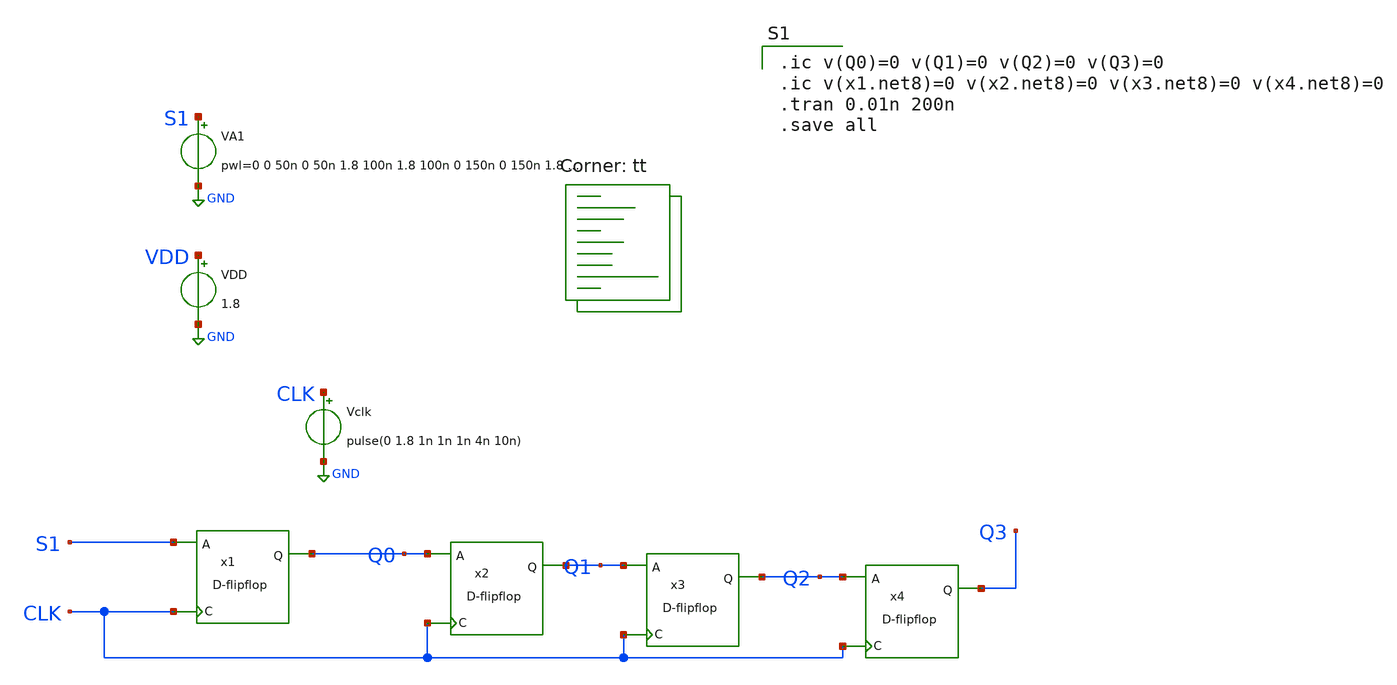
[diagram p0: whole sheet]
** sch_path: gates/dflipshift4bitsim.sch
**.subckt dflipshift4bitsim
x1 S1 Q0 CLK D-flipflop
x2 Q0 Q1 CLK D-flipflop
x3 Q1 Q2 CLK D-flipflop
x4 Q2 Q3 CLK D-flipflop
Vclk CLK GND pulse(0 1.8 1n 1n 1n 4n 10n)
VDD VDD GND 1.8
VA1 S1 GND pwl=0 0 50n 0 50n 1.8 100n 1.8 100n 0 150n 0 150n 1.8 200n 1.8
**** begin user architecture code
.lib $::SKYWATER_MODELS/sky130.lib.spice tt

.ic v(Q0)=0 v(Q1)=0 v(Q2)=0 v(Q3)=0
.ic v(x1.net8)=0 v(x2.net8)=0 v(x3.net8)=0 v(x4.net8)=0
.tran 0.01n 200n
.save all

**** end user architecture code
**.ends

* expanding   symbol:  D-flipflop.sym # of pins=3
** sym_path: gates/D-flipflop.sym
** sch_path: gates/D-flipflop.sch
.subckt D-flipflop A Q C
*.ipin A
*.ipin C
*.opin Q
x1 A net1 C NAND2_Gate
x2 net3 net2 C NAND2_Gate
x3 net1 Q Q' NAND2_Gate
x4 net2 Q' Q NAND2_Gate
X5 A net3 inv_vtc
.ends


* expanding   symbol:  NAND2_Gate.sym # of pins=3
** sym_path: gates/NAND2_Gate.sym
** sch_path: gates/NAND2_Gate.sch
.subckt NAND2_Gate A Y B
*.ipin A
*.ipin B
*.opin Y
XM1 Y A net1 GND sky130_fd_pr__nfet_01v8 L=0.15 W=1 nf=1 ad='int((nf+1)/2) * W/nf * 0.29' as='int((nf+2)/2) * W/nf * 0.29'
+ pd='2*int((nf+1)/2) * (W/nf + 0.29)' ps='2*int((nf+2)/2) * (W/nf + 0.29)' nrd='0.29 / W' nrs='0.29 / W'
+ sa=0 sb=0 sd=0 mult=1 m=1
XM2 net1 B GND GND sky130_fd_pr__nfet_01v8 L=0.15 W=1 nf=1 ad='int((nf+1)/2) * W/nf * 0.29' as='int((nf+2)/2) * W/nf * 0.29'
+ pd='2*int((nf+1)/2) * (W/nf + 0.29)' ps='2*int((nf+2)/2) * (W/nf + 0.29)' nrd='0.29 / W' nrs='0.29 / W'
+ sa=0 sb=0 sd=0 mult=1 m=1
XM3 Y A VDD VDD sky130_fd_pr__pfet_01v8 L=0.15 W=1 nf=1 ad='int((nf+1)/2) * W/nf * 0.29' as='int((nf+2)/2) * W/nf * 0.29'
+ pd='2*int((nf+1)/2) * (W/nf + 0.29)' ps='2*int((nf+2)/2) * (W/nf + 0.29)' nrd='0.29 / W' nrs='0.29 / W'
+ sa=0 sb=0 sd=0 mult=1 m=1
XM4 Y B VDD VDD sky130_fd_pr__pfet_01v8 L=0.15 W=1 nf=1 ad='int((nf+1)/2) * W/nf * 0.29' as='int((nf+2)/2) * W/nf * 0.29'
+ pd='2*int((nf+1)/2) * (W/nf + 0.29)' ps='2*int((nf+2)/2) * (W/nf + 0.29)' nrd='0.29 / W' nrs='0.29 / W'
+ sa=0 sb=0 sd=0 mult=1 m=1
.ends


* expanding   symbol:  /home/apn/test_xschem_sky130/inv_vtc.sym # of pins=2
** sym_path: gates/inv_vtc.sym
** sch_path: gates/inv_vtc.sch
.subckt inv_vtc A Y
*.ipin A
*.opin Y
XM1 Y A VDD VDD sky130_fd_pr__pfet_01v8 L=0.15 W=2 nf=1 ad='int((nf+1)/2) * W/nf * 0.29' as='int((nf+2)/2) * W/nf * 0.29'
+ pd='2*int((nf+1)/2) * (W/nf + 0.29)' ps='2*int((nf+2)/2) * (W/nf + 0.29)' nrd='0.29 / W' nrs='0.29 / W'
+ sa=0 sb=0 sd=0 mult=1 m=1
XM2 Y A GND GND sky130_fd_pr__nfet_01v8 L=0.15 W=1 nf=1 ad='int((nf+1)/2) * W/nf * 0.29' as='int((nf+2)/2) * W/nf * 0.29'
+ pd='2*int((nf+1)/2) * (W/nf + 0.29)' ps='2*int((nf+2)/2) * (W/nf + 0.29)' nrd='0.29 / W' nrs='0.29 / W'
+ sa=0 sb=0 sd=0 mult=1 m=1
.ends

.GLOBAL GND
.GLOBAL VDD
.end
